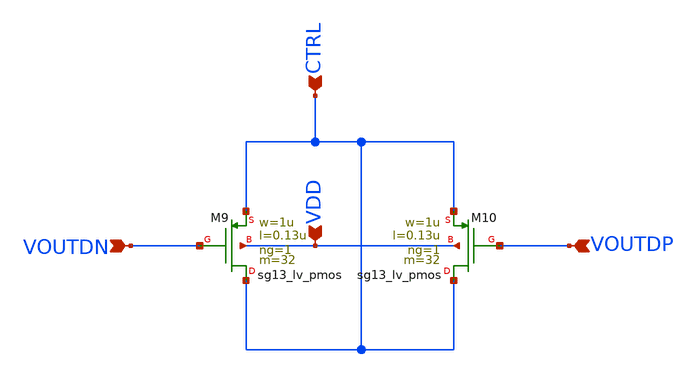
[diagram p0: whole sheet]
** sch_path: Clock_Gen/decap.sch
**.subckt decap CTRL VDD VOUTDN VOUTDP
*.ipin CTRL
*.ipin VDD
*.ipin VOUTDN
*.ipin VOUTDP
XM10 CTRL VOUTDP CTRL VDD sg13_lv_pmos w=1u l=0.13u ng=1 m=32 mm_ok=1
XM9 CTRL VOUTDN CTRL VDD sg13_lv_pmos w=1u l=0.13u ng=1 m=32 mm_ok=1
**.ends
.end
